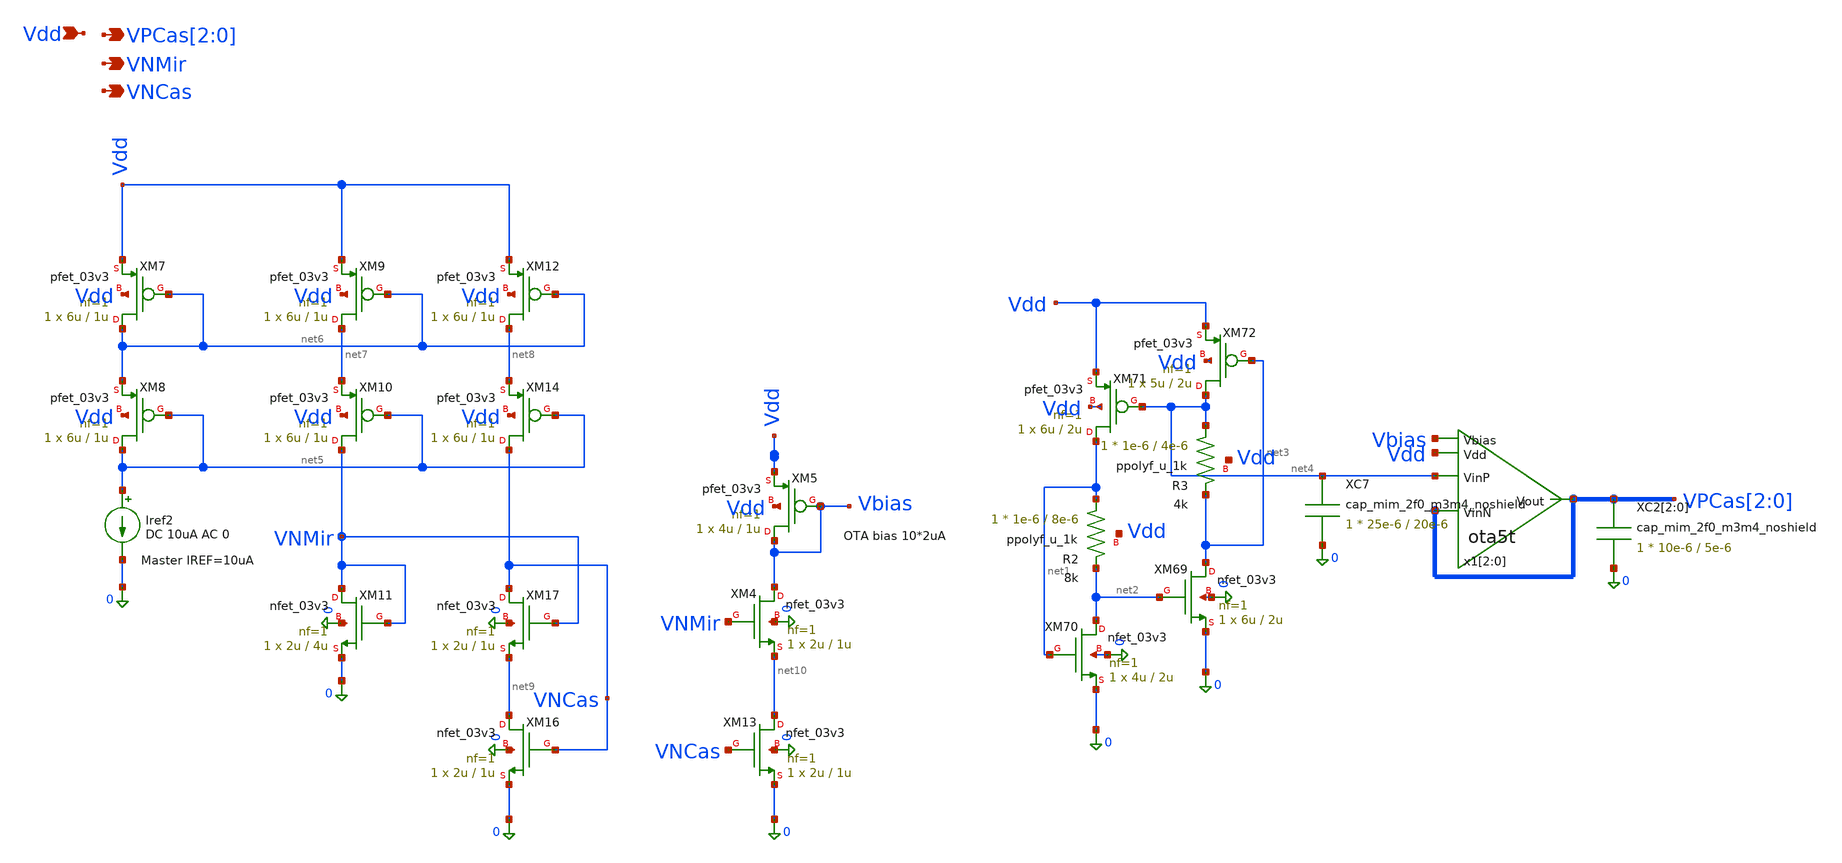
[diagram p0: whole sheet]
** sch_path: blocks/dac/iref/dac_iref.sch
**.subckt dac_iref Vdd VPCas[2],VPCas[1],VPCas[0] VNMir VNCas
*.ipin Vdd
*.opin VPCas[2],VPCas[1],VPCas[0]
*.opin VNMir
*.opin VNCas
XM69 net3 net2 0 0 nfet_03v3 L=2u W=6u nf=1 ad='int((nf+1)/2) * W/nf * 0.18u' as='int((nf+2)/2) * W/nf * 0.18u'
+ pd='2*int((nf+1)/2) * (W/nf + 0.18u)' ps='2*int((nf+2)/2) * (W/nf + 0.18u)' nrd='0.18u / W' nrs='0.18u / W'
+ sa=0 sb=0 sd=0 m=1
XM70 net2 net1 0 0 nfet_03v3 L=2u W=4u nf=1 ad='int((nf+1)/2) * W/nf * 0.18u' as='int((nf+2)/2) * W/nf * 0.18u'
+ pd='2*int((nf+1)/2) * (W/nf + 0.18u)' ps='2*int((nf+2)/2) * (W/nf + 0.18u)' nrd='0.18u / W' nrs='0.18u / W'
+ sa=0 sb=0 sd=0 m=1
XM71 net1 net4 Vdd Vdd pfet_03v3 L=2u W=6u nf=1 ad='int((nf+1)/2) * W/nf * 0.18u' as='int((nf+2)/2) * W/nf * 0.18u'
+ pd='2*int((nf+1)/2) * (W/nf + 0.18u)' ps='2*int((nf+2)/2) * (W/nf + 0.18u)' nrd='0.18u / W' nrs='0.18u / W'
+ sa=0 sb=0 sd=0 m=1
XM72 net4 net3 Vdd Vdd pfet_03v3 L=2u W=5u nf=1 ad='int((nf+1)/2) * W/nf * 0.18u' as='int((nf+2)/2) * W/nf * 0.18u'
+ pd='2*int((nf+1)/2) * (W/nf + 0.18u)' ps='2*int((nf+2)/2) * (W/nf + 0.18u)' nrd='0.18u / W' nrs='0.18u / W'
+ sa=0 sb=0 sd=0 m=1
x1[2] Vdd VPCas[2] net4 VPCas[2] Vbias ota5t
x1[1] Vdd VPCas[1] net4 VPCas[1] Vbias ota5t
x1[0] Vdd VPCas[0] net4 VPCas[0] Vbias ota5t
XC7 net4 0 cap_mim_2f0_m3m4_noshield c_width=25e-6 c_length=20e-6 m=1
XC2[2] VPCas[2] 0 cap_mim_2f0_m3m4_noshield c_width=10e-6 c_length=5e-6 m=1
XC2[1] VPCas[1] 0 cap_mim_2f0_m3m4_noshield c_width=10e-6 c_length=5e-6 m=1
XC2[0] VPCas[0] 0 cap_mim_2f0_m3m4_noshield c_width=10e-6 c_length=5e-6 m=1
XM7 net6 net6 Vdd Vdd pfet_03v3 L=1u W=6u nf=1 ad='int((nf+1)/2) * W/nf * 0.18u' as='int((nf+2)/2) * W/nf * 0.18u'
+ pd='2*int((nf+1)/2) * (W/nf + 0.18u)' ps='2*int((nf+2)/2) * (W/nf + 0.18u)' nrd='0.18u / W' nrs='0.18u / W'
+ sa=0 sb=0 sd=0 m=1
XM8 net5 net5 net6 Vdd pfet_03v3 L=1u W=6u nf=1 ad='int((nf+1)/2) * W/nf * 0.18u' as='int((nf+2)/2) * W/nf * 0.18u'
+ pd='2*int((nf+1)/2) * (W/nf + 0.18u)' ps='2*int((nf+2)/2) * (W/nf + 0.18u)' nrd='0.18u / W' nrs='0.18u / W'
+ sa=0 sb=0 sd=0 m=1
Iref2 net5 0 DC 10uA AC 0
XM9 net7 net6 Vdd Vdd pfet_03v3 L=1u W=6u nf=1 ad='int((nf+1)/2) * W/nf * 0.18u' as='int((nf+2)/2) * W/nf * 0.18u'
+ pd='2*int((nf+1)/2) * (W/nf + 0.18u)' ps='2*int((nf+2)/2) * (W/nf + 0.18u)' nrd='0.18u / W' nrs='0.18u / W'
+ sa=0 sb=0 sd=0 m=1
XM10 VNMir net5 net7 Vdd pfet_03v3 L=1u W=6u nf=1 ad='int((nf+1)/2) * W/nf * 0.18u' as='int((nf+2)/2) * W/nf * 0.18u'
+ pd='2*int((nf+1)/2) * (W/nf + 0.18u)' ps='2*int((nf+2)/2) * (W/nf + 0.18u)' nrd='0.18u / W' nrs='0.18u / W'
+ sa=0 sb=0 sd=0 m=1
XM11 VNMir VNMir 0 0 nfet_03v3 L=4u W=2u nf=1 ad='int((nf+1)/2) * W/nf * 0.18u' as='int((nf+2)/2) * W/nf * 0.18u'
+ pd='2*int((nf+1)/2) * (W/nf + 0.18u)' ps='2*int((nf+2)/2) * (W/nf + 0.18u)' nrd='0.18u / W' nrs='0.18u / W'
+ sa=0 sb=0 sd=0 m=1
XM12 net8 net6 Vdd Vdd pfet_03v3 L=1u W=6u nf=1 ad='int((nf+1)/2) * W/nf * 0.18u' as='int((nf+2)/2) * W/nf * 0.18u'
+ pd='2*int((nf+1)/2) * (W/nf + 0.18u)' ps='2*int((nf+2)/2) * (W/nf + 0.18u)' nrd='0.18u / W' nrs='0.18u / W'
+ sa=0 sb=0 sd=0 m=1
XM14 VNCas net5 net8 Vdd pfet_03v3 L=1u W=6u nf=1 ad='int((nf+1)/2) * W/nf * 0.18u' as='int((nf+2)/2) * W/nf * 0.18u'
+ pd='2*int((nf+1)/2) * (W/nf + 0.18u)' ps='2*int((nf+2)/2) * (W/nf + 0.18u)' nrd='0.18u / W' nrs='0.18u / W'
+ sa=0 sb=0 sd=0 m=1
XM16 net9 VNCas 0 0 nfet_03v3 L=1u W=2u nf=1 ad='int((nf+1)/2) * W/nf * 0.18u' as='int((nf+2)/2) * W/nf * 0.18u'
+ pd='2*int((nf+1)/2) * (W/nf + 0.18u)' ps='2*int((nf+2)/2) * (W/nf + 0.18u)' nrd='0.18u / W' nrs='0.18u / W'
+ sa=0 sb=0 sd=0 m=1
XM17 VNCas VNMir net9 0 nfet_03v3 L=1u W=2u nf=1 ad='int((nf+1)/2) * W/nf * 0.18u' as='int((nf+2)/2) * W/nf * 0.18u'
+ pd='2*int((nf+1)/2) * (W/nf + 0.18u)' ps='2*int((nf+2)/2) * (W/nf + 0.18u)' nrd='0.18u / W' nrs='0.18u / W'
+ sa=0 sb=0 sd=0 m=1
XM4 Vbias VNMir net10 0 nfet_03v3 L=1u W=2u nf=1 ad='int((nf+1)/2) * W/nf * 0.18u' as='int((nf+2)/2) * W/nf * 0.18u'
+ pd='2*int((nf+1)/2) * (W/nf + 0.18u)' ps='2*int((nf+2)/2) * (W/nf + 0.18u)' nrd='0.18u / W' nrs='0.18u / W'
+ sa=0 sb=0 sd=0 m=1
XM5 Vbias Vbias Vdd Vdd pfet_03v3 L=1u W=4u nf=1 ad='int((nf+1)/2) * W/nf * 0.18u' as='int((nf+2)/2) * W/nf * 0.18u'
+ pd='2*int((nf+1)/2) * (W/nf + 0.18u)' ps='2*int((nf+2)/2) * (W/nf + 0.18u)' nrd='0.18u / W' nrs='0.18u / W'
+ sa=0 sb=0 sd=0 m=1
XM13 net10 VNCas 0 0 nfet_03v3 L=1u W=2u nf=1 ad='int((nf+1)/2) * W/nf * 0.18u' as='int((nf+2)/2) * W/nf * 0.18u'
+ pd='2*int((nf+1)/2) * (W/nf + 0.18u)' ps='2*int((nf+2)/2) * (W/nf + 0.18u)' nrd='0.18u / W' nrs='0.18u / W'
+ sa=0 sb=0 sd=0 m=1
XR3 net4 net3 Vdd ppolyf_u_1k r_width=1e-6 r_length=4e-6 m=1
XR2 net1 net2 Vdd ppolyf_u_1k r_width=1e-6 r_length=8e-6 m=1
**.ends

* expanding   symbol:  common/ota5t.sym # of pins=5
** sym_path: blocks/dac/common/ota5t.sym
** sch_path: blocks/dac/common/ota5t.sch
.subckt ota5t Vdd VinN VinP Vout Vbias
*.ipin VinP
*.ipin VinN
*.opin Vout
*.ipin Vdd
*.ipin Vbias
XM16 Vout net2 0 0 nfet_03v3 L=1u W=2u nf=1 ad='int((nf+1)/2) * W/nf * 0.18u' as='int((nf+2)/2) * W/nf * 0.18u'
+ pd='2*int((nf+1)/2) * (W/nf + 0.18u)' ps='2*int((nf+2)/2) * (W/nf + 0.18u)' nrd='0.18u / W' nrs='0.18u / W'
+ sa=0 sb=0 sd=0 m=1
XM1 Vout VinN net1 Vdd pfet_03v3 L=1u W=4u nf=1 ad='int((nf+1)/2) * W/nf * 0.18u' as='int((nf+2)/2) * W/nf * 0.18u'
+ pd='2*int((nf+1)/2) * (W/nf + 0.18u)' ps='2*int((nf+2)/2) * (W/nf + 0.18u)' nrd='0.18u / W' nrs='0.18u / W'
+ sa=0 sb=0 sd=0 m=1
XM19 net2 VinP net1 Vdd pfet_03v3 L=1u W=4u nf=1 ad='int((nf+1)/2) * W/nf * 0.18u' as='int((nf+2)/2) * W/nf * 0.18u'
+ pd='2*int((nf+1)/2) * (W/nf + 0.18u)' ps='2*int((nf+2)/2) * (W/nf + 0.18u)' nrd='0.18u / W' nrs='0.18u / W'
+ sa=0 sb=0 sd=0 m=1
XM22 net2 net2 0 0 nfet_03v3 L=1u W=2u nf=1 ad='int((nf+1)/2) * W/nf * 0.18u' as='int((nf+2)/2) * W/nf * 0.18u'
+ pd='2*int((nf+1)/2) * (W/nf + 0.18u)' ps='2*int((nf+2)/2) * (W/nf + 0.18u)' nrd='0.18u / W' nrs='0.18u / W'
+ sa=0 sb=0 sd=0 m=1
.param bbW=2u
.param bbL=1u
XM29 net1 Vbias Vdd Vdd pfet_03v3 L=1u W=4u nf=1 ad='int((nf+1)/2) * W/nf * 0.18u' as='int((nf+2)/2) * W/nf * 0.18u'
+ pd='2*int((nf+1)/2) * (W/nf + 0.18u)' ps='2*int((nf+2)/2) * (W/nf + 0.18u)' nrd='0.18u / W' nrs='0.18u / W'
+ sa=0 sb=0 sd=0 m=2
.ends

.end
